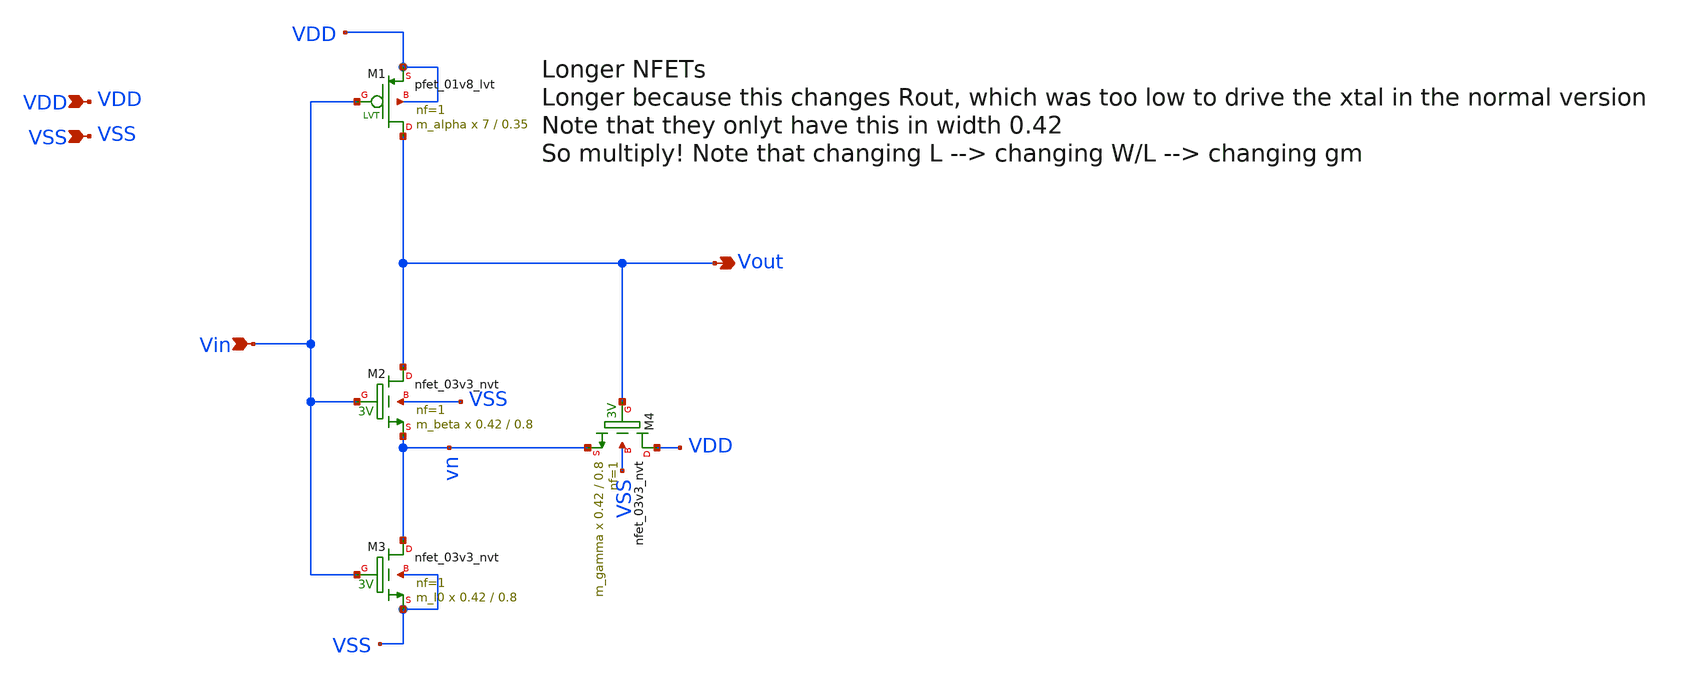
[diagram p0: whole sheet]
** sch_path: design/THESIS_EXP_RO_INVERTER_SKY130A/INV_NVT_feedback_long.sch
**.subckt INV_NVT_feedback_long VSS Vin Vout VDD
*.ipin VSS
*.ipin Vin
*.opin Vout
*.ipin VDD
XM1 Vout Vin VDD VDD sky130_fd_pr__pfet_01v8_lvt L=0.35 W=7 nf=1 ad='int((nf+1)/2) * W/nf * 0.29' as='int((nf+2)/2) * W/nf * 0.29'
+ pd='2*int((nf+1)/2) * (W/nf + 0.29)' ps='2*int((nf+2)/2) * (W/nf + 0.29)' nrd='0.29 / W' nrs='0.29 / W'
+ sa=0 sb=0 sd=0 mult=m_alpha m=m_alpha
XM2 Vout Vin vn VSS sky130_fd_pr__nfet_03v3_nvt L=0.8 W=0.42 nf=1 ad='int((nf+1)/2) * W/nf * 0.29' as='int((nf+2)/2) * W/nf * 0.29'
+ pd='2*int((nf+1)/2) * (W/nf + 0.29)' ps='2*int((nf+2)/2) * (W/nf + 0.29)' nrd='0.29 / W' nrs='0.29 / W'
+ sa=0 sb=0 sd=0 mult=m_beta m=m_beta
XM3 vn Vin VSS VSS sky130_fd_pr__nfet_03v3_nvt L=0.8 W=0.42 nf=1 ad='int((nf+1)/2) * W/nf * 0.29' as='int((nf+2)/2) * W/nf * 0.29'
+ pd='2*int((nf+1)/2) * (W/nf + 0.29)' ps='2*int((nf+2)/2) * (W/nf + 0.29)' nrd='0.29 / W' nrs='0.29 / W'
+ sa=0 sb=0 sd=0 mult=m_I0 m=m_I0
XM4 VDD Vout vn VSS sky130_fd_pr__nfet_03v3_nvt L=0.8 W=0.42 nf=1 ad='int((nf+1)/2) * W/nf * 0.29' as='int((nf+2)/2) * W/nf * 0.29'
+ pd='2*int((nf+1)/2) * (W/nf + 0.29)' ps='2*int((nf+2)/2) * (W/nf + 0.29)' nrd='0.29 / W' nrs='0.29 / W'
+ sa=0 sb=0 sd=0 mult=m_gamma m=m_gamma
**.ends
.end
